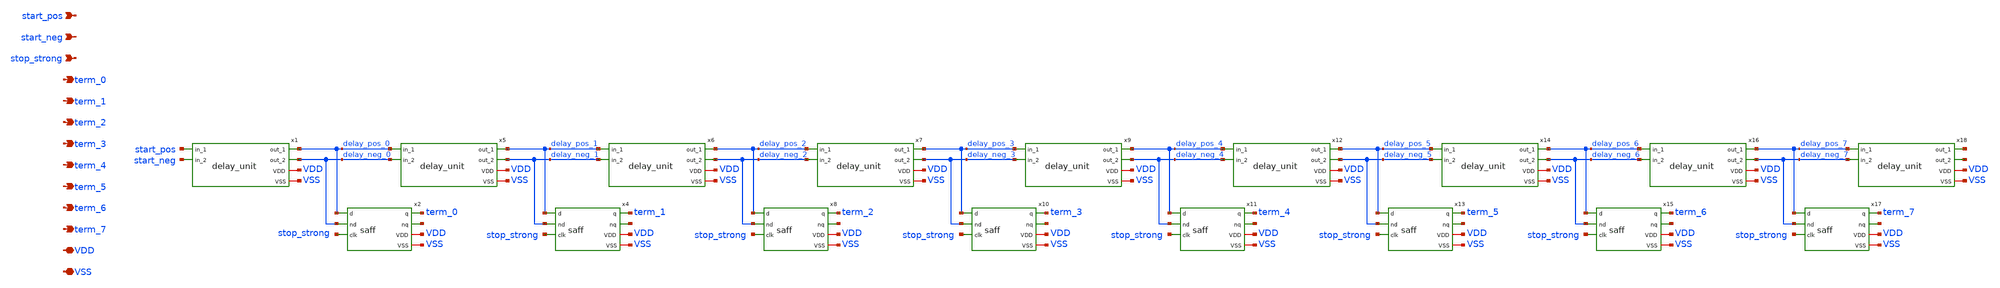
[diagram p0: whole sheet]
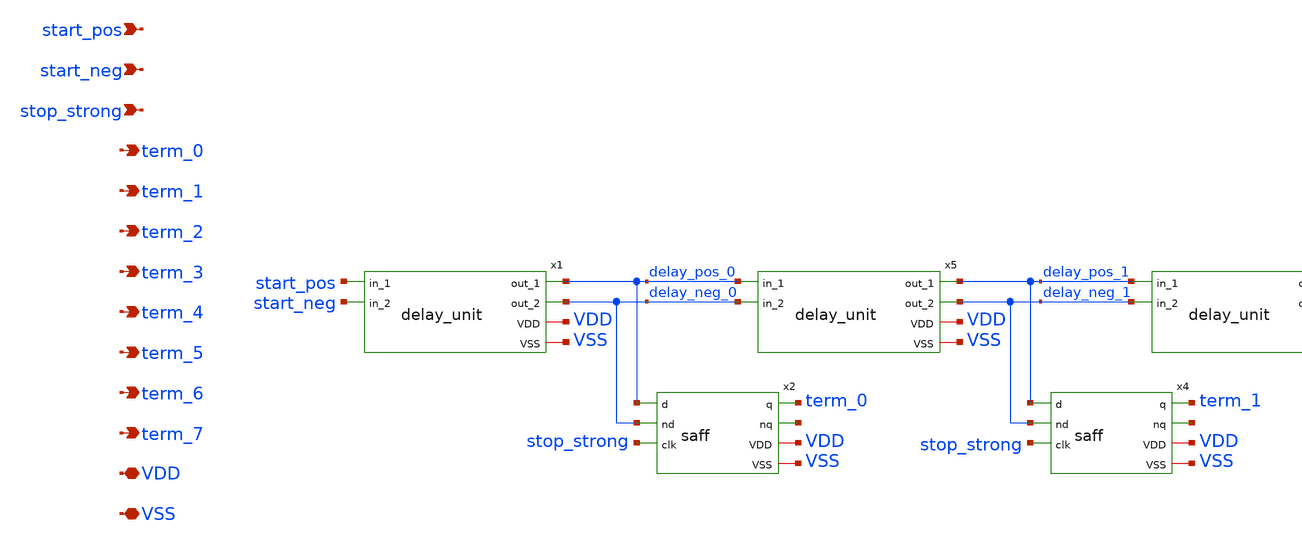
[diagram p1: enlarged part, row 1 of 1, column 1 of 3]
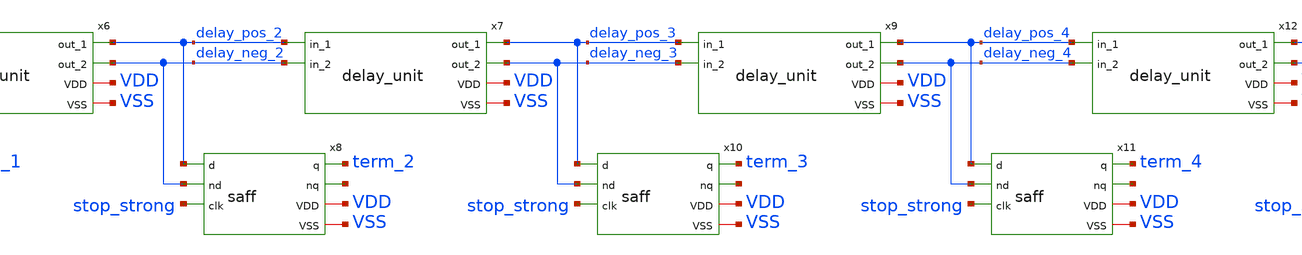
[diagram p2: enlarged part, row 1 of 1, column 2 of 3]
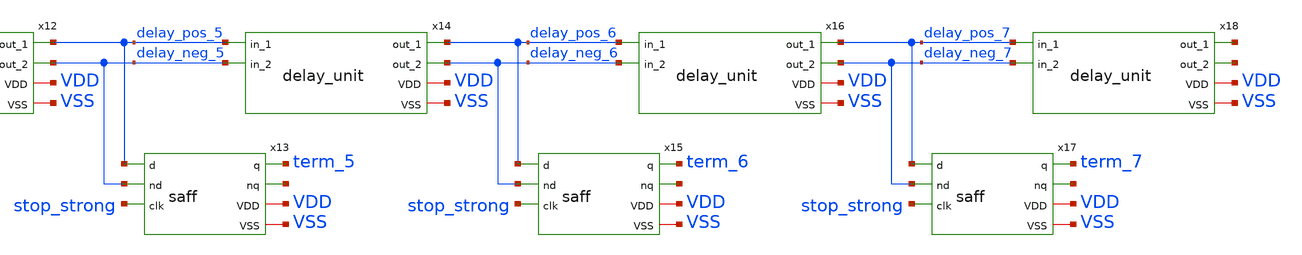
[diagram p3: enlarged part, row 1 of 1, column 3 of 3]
** sch_path: xschem/vernier_delay_line.sch
**.subckt vernier_delay_line VDD VSS start_pos stop_strong term_0 term_1 term_2 term_3 term_4 term_5
*+ term_6 term_7 start_neg
*.iopin VDD
*.iopin VSS
*.ipin start_pos
*.ipin stop_strong
*.opin term_0
*.opin term_1
*.opin term_2
*.opin term_3
*.opin term_4
*.opin term_5
*.opin term_6
*.opin term_7
*.ipin start_neg
x1 delay_pos_0 start_pos start_neg VDD delay_neg_0 VSS delay_unit
x2 delay_pos_0 delay_neg_0 stop_strong term_0 net1 VDD VSS saff
x4 delay_pos_1 delay_neg_1 stop_strong term_1 net2 VDD VSS saff
x5 delay_pos_1 delay_pos_0 delay_neg_0 VDD delay_neg_1 VSS delay_unit
x6 delay_pos_2 delay_pos_1 delay_neg_1 VDD delay_neg_2 VSS delay_unit
x7 delay_pos_3 delay_pos_2 delay_neg_2 VDD delay_neg_3 VSS delay_unit
x8 delay_pos_2 delay_neg_2 stop_strong term_2 net3 VDD VSS saff
x9 delay_pos_4 delay_pos_3 delay_neg_3 VDD delay_neg_4 VSS delay_unit
x10 delay_pos_3 delay_neg_3 stop_strong term_3 net4 VDD VSS saff
x11 delay_pos_4 delay_neg_4 stop_strong term_4 net5 VDD VSS saff
x12 delay_pos_5 delay_pos_4 delay_neg_4 VDD delay_neg_5 VSS delay_unit
x13 delay_pos_5 delay_neg_5 stop_strong term_5 net6 VDD VSS saff
x14 delay_pos_6 delay_pos_5 delay_neg_5 VDD delay_neg_6 VSS delay_unit
x15 delay_pos_6 delay_neg_6 stop_strong term_6 net7 VDD VSS saff
x16 delay_pos_7 delay_pos_6 delay_neg_6 VDD delay_neg_7 VSS delay_unit
x17 delay_pos_7 delay_neg_7 stop_strong term_7 net8 VDD VSS saff
x18 net9 delay_pos_7 delay_neg_7 VDD net10 VSS delay_unit
**.ends

* expanding   symbol:  delay_unit.sym # of pins=6
** sym_path: xschem/delay_unit.sym
** sch_path: xschem/delay_unit.sch
.subckt delay_unit out_1 in_1 in_2 VDD out_2 VSS
*.iopin VDD
*.ipin in_1
*.opin out_1
*.iopin VSS
*.ipin in_2
*.opin out_2
XM5 out_2 in_1 VDD VDD sky130_fd_pr__pfet_01v8 L=0.15 W=9 nf=1 ad='int((nf+1)/2) * W/nf * 0.29' as='int((nf+2)/2) * W/nf * 0.29'
+ pd='2*int((nf+1)/2) * (W/nf + 0.29)' ps='2*int((nf+2)/2) * (W/nf + 0.29)' nrd='0.29 / W' nrs='0.29 / W'
+ sa=0 sb=0 sd=0 mult=1 m=1
XM7 out_2 in_1 VSS VSS sky130_fd_pr__nfet_01v8 L=0.15 W=3 nf=1 ad='int((nf+1)/2) * W/nf * 0.29' as='int((nf+2)/2) * W/nf * 0.29'
+ pd='2*int((nf+1)/2) * (W/nf + 0.29)' ps='2*int((nf+2)/2) * (W/nf + 0.29)' nrd='0.29 / W' nrs='0.29 / W'
+ sa=0 sb=0 sd=0 mult=1 m=1
XM1 out_1 in_2 VDD VDD sky130_fd_pr__pfet_01v8 L=0.15 W=9 nf=1 ad='int((nf+1)/2) * W/nf * 0.29' as='int((nf+2)/2) * W/nf * 0.29'
+ pd='2*int((nf+1)/2) * (W/nf + 0.29)' ps='2*int((nf+2)/2) * (W/nf + 0.29)' nrd='0.29 / W' nrs='0.29 / W'
+ sa=0 sb=0 sd=0 mult=1 m=1
XM2 out_1 in_2 VSS VSS sky130_fd_pr__nfet_01v8 L=0.15 W=3 nf=1 ad='int((nf+1)/2) * W/nf * 0.29' as='int((nf+2)/2) * W/nf * 0.29'
+ pd='2*int((nf+1)/2) * (W/nf + 0.29)' ps='2*int((nf+2)/2) * (W/nf + 0.29)' nrd='0.29 / W' nrs='0.29 / W'
+ sa=0 sb=0 sd=0 mult=1 m=1
XM3 in_1 in_2 VDD VDD sky130_fd_pr__pfet_01v8 L=0.15 W=3 nf=1 ad='int((nf+1)/2) * W/nf * 0.29' as='int((nf+2)/2) * W/nf * 0.29'
+ pd='2*int((nf+1)/2) * (W/nf + 0.29)' ps='2*int((nf+2)/2) * (W/nf + 0.29)' nrd='0.29 / W' nrs='0.29 / W'
+ sa=0 sb=0 sd=0 mult=1 m=1
XM4 in_1 in_2 VSS VSS sky130_fd_pr__nfet_01v8 L=0.15 W=1 nf=1 ad='int((nf+1)/2) * W/nf * 0.29' as='int((nf+2)/2) * W/nf * 0.29'
+ pd='2*int((nf+1)/2) * (W/nf + 0.29)' ps='2*int((nf+2)/2) * (W/nf + 0.29)' nrd='0.29 / W' nrs='0.29 / W'
+ sa=0 sb=0 sd=0 mult=1 m=1
XM6 in_2 in_1 VDD VDD sky130_fd_pr__pfet_01v8 L=0.15 W=3 nf=1 ad='int((nf+1)/2) * W/nf * 0.29' as='int((nf+2)/2) * W/nf * 0.29'
+ pd='2*int((nf+1)/2) * (W/nf + 0.29)' ps='2*int((nf+2)/2) * (W/nf + 0.29)' nrd='0.29 / W' nrs='0.29 / W'
+ sa=0 sb=0 sd=0 mult=1 m=1
XM8 in_2 in_1 VSS VSS sky130_fd_pr__nfet_01v8 L=0.15 W=1 nf=1 ad='int((nf+1)/2) * W/nf * 0.29' as='int((nf+2)/2) * W/nf * 0.29'
+ pd='2*int((nf+1)/2) * (W/nf + 0.29)' ps='2*int((nf+2)/2) * (W/nf + 0.29)' nrd='0.29 / W' nrs='0.29 / W'
+ sa=0 sb=0 sd=0 mult=1 m=1
.ends


* expanding   symbol:  saff.sym # of pins=7
** sym_path: xschem/saff.sym
** sch_path: xschem/saff.sch
.subckt saff d nd clk q nq VDD VSS
*.iopin VDD
*.ipin d
*.opin q
*.iopin VSS
*.ipin nd
*.ipin clk
*.opin nq
XM2 net3 q VSS VSS sky130_fd_pr__nfet_01v8 L=0.15 W=1 nf=1 ad='int((nf+1)/2) * W/nf * 0.29' as='int((nf+2)/2) * W/nf * 0.29'
+ pd='2*int((nf+1)/2) * (W/nf + 0.29)' ps='2*int((nf+2)/2) * (W/nf + 0.29)' nrd='0.29 / W' nrs='0.29 / W'
+ sa=0 sb=0 sd=0 mult=1 m=1
XM3 left_latch_1 clk VDD VDD sky130_fd_pr__pfet_01v8 L=0.15 W=3 nf=1 ad='int((nf+1)/2) * W/nf * 0.29'
+ as='int((nf+2)/2) * W/nf * 0.29' pd='2*int((nf+1)/2) * (W/nf + 0.29)' ps='2*int((nf+2)/2) * (W/nf + 0.29)'
+ nrd='0.29 / W' nrs='0.29 / W' sa=0 sb=0 sd=0 mult=1 m=1
XM4 right_latch_1 clk VDD VDD sky130_fd_pr__pfet_01v8 L=0.15 W=3 nf=1 ad='int((nf+1)/2) * W/nf * 0.29'
+ as='int((nf+2)/2) * W/nf * 0.29' pd='2*int((nf+1)/2) * (W/nf + 0.29)' ps='2*int((nf+2)/2) * (W/nf + 0.29)'
+ nrd='0.29 / W' nrs='0.29 / W' sa=0 sb=0 sd=0 mult=1 m=1
XM5 right_latch_1 left_latch_1 VDD VDD sky130_fd_pr__pfet_01v8 L=0.15 W=3 nf=1 ad='int((nf+1)/2) * W/nf * 0.29'
+ as='int((nf+2)/2) * W/nf * 0.29' pd='2*int((nf+1)/2) * (W/nf + 0.29)' ps='2*int((nf+2)/2) * (W/nf + 0.29)'
+ nrd='0.29 / W' nrs='0.29 / W' sa=0 sb=0 sd=0 mult=1 m=1
XM6 left_latch_1 right_latch_1 VDD VDD sky130_fd_pr__pfet_01v8 L=0.15 W=3 nf=1 ad='int((nf+1)/2) * W/nf * 0.29'
+ as='int((nf+2)/2) * W/nf * 0.29' pd='2*int((nf+1)/2) * (W/nf + 0.29)' ps='2*int((nf+2)/2) * (W/nf + 0.29)'
+ nrd='0.29 / W' nrs='0.29 / W' sa=0 sb=0 sd=0 mult=1 m=1
XM7 right_latch_1 left_latch_1 net7 VSS sky130_fd_pr__nfet_01v8 L=0.15 W=6 nf=1 ad='int((nf+1)/2) * W/nf * 0.29'
+ as='int((nf+2)/2) * W/nf * 0.29' pd='2*int((nf+1)/2) * (W/nf + 0.29)' ps='2*int((nf+2)/2) * (W/nf + 0.29)'
+ nrd='0.29 / W' nrs='0.29 / W' sa=0 sb=0 sd=0 mult=1 m=1
XM8 left_latch_1 right_latch_1 net5 VSS sky130_fd_pr__nfet_01v8 L=0.15 W=6 nf=1 ad='int((nf+1)/2) * W/nf * 0.29'
+ as='int((nf+2)/2) * W/nf * 0.29' pd='2*int((nf+1)/2) * (W/nf + 0.29)' ps='2*int((nf+2)/2) * (W/nf + 0.29)'
+ nrd='0.29 / W' nrs='0.29 / W' sa=0 sb=0 sd=0 mult=1 m=1
XM9 net6 clk VSS VSS sky130_fd_pr__nfet_01v8 L=0.15 W=15 nf=1 ad='int((nf+1)/2) * W/nf * 0.29' as='int((nf+2)/2) * W/nf * 0.29'
+ pd='2*int((nf+1)/2) * (W/nf + 0.29)' ps='2*int((nf+2)/2) * (W/nf + 0.29)' nrd='0.29 / W' nrs='0.29 / W'
+ sa=0 sb=0 sd=0 mult=1 m=1
XM10 net7 nd net6 VSS sky130_fd_pr__nfet_01v8 L=0.15 W=12 nf=1 ad='int((nf+1)/2) * W/nf * 0.29' as='int((nf+2)/2) * W/nf * 0.29'
+ pd='2*int((nf+1)/2) * (W/nf + 0.29)' ps='2*int((nf+2)/2) * (W/nf + 0.29)' nrd='0.29 / W' nrs='0.29 / W'
+ sa=0 sb=0 sd=0 mult=1 m=1
XM11 net5 d net6 VSS sky130_fd_pr__nfet_01v8 L=0.15 W=12 nf=1 ad='int((nf+1)/2) * W/nf * 0.29' as='int((nf+2)/2) * W/nf * 0.29'
+ pd='2*int((nf+1)/2) * (W/nf + 0.29)' ps='2*int((nf+2)/2) * (W/nf + 0.29)' nrd='0.29 / W' nrs='0.29 / W'
+ sa=0 sb=0 sd=0 mult=1 m=1
XM12 right_latch_2 left_latch_1 VDD VDD sky130_fd_pr__pfet_01v8 L=0.15 W=6 nf=1 ad='int((nf+1)/2) * W/nf * 0.29'
+ as='int((nf+2)/2) * W/nf * 0.29' pd='2*int((nf+1)/2) * (W/nf + 0.29)' ps='2*int((nf+2)/2) * (W/nf + 0.29)'
+ nrd='0.29 / W' nrs='0.29 / W' sa=0 sb=0 sd=0 mult=1 m=1
XM13 right_latch_2 left_latch_1 VSS VSS sky130_fd_pr__nfet_01v8 L=0.15 W=2 nf=1 ad='int((nf+1)/2) * W/nf * 0.29'
+ as='int((nf+2)/2) * W/nf * 0.29' pd='2*int((nf+1)/2) * (W/nf + 0.29)' ps='2*int((nf+2)/2) * (W/nf + 0.29)'
+ nrd='0.29 / W' nrs='0.29 / W' sa=0 sb=0 sd=0 mult=1 m=1
XM14 left_latch_2 right_latch_1 VDD VDD sky130_fd_pr__pfet_01v8 L=0.15 W=6 nf=1 ad='int((nf+1)/2) * W/nf * 0.29'
+ as='int((nf+2)/2) * W/nf * 0.29' pd='2*int((nf+1)/2) * (W/nf + 0.29)' ps='2*int((nf+2)/2) * (W/nf + 0.29)'
+ nrd='0.29 / W' nrs='0.29 / W' sa=0 sb=0 sd=0 mult=1 m=1
XM15 left_latch_2 right_latch_1 VSS VSS sky130_fd_pr__nfet_01v8 L=0.15 W=2 nf=1 ad='int((nf+1)/2) * W/nf * 0.29'
+ as='int((nf+2)/2) * W/nf * 0.29' pd='2*int((nf+1)/2) * (W/nf + 0.29)' ps='2*int((nf+2)/2) * (W/nf + 0.29)'
+ nrd='0.29 / W' nrs='0.29 / W' sa=0 sb=0 sd=0 mult=1 m=1
XM16 q left_latch_1 VDD VDD sky130_fd_pr__pfet_01v8 L=0.15 W=3 nf=1 ad='int((nf+1)/2) * W/nf * 0.29'
+ as='int((nf+2)/2) * W/nf * 0.29' pd='2*int((nf+1)/2) * (W/nf + 0.29)' ps='2*int((nf+2)/2) * (W/nf + 0.29)'
+ nrd='0.29 / W' nrs='0.29 / W' sa=0 sb=0 sd=0 mult=1 m=1
XM17 q left_latch_2 VSS VSS sky130_fd_pr__nfet_01v8 L=0.15 W=1 nf=1 ad='int((nf+1)/2) * W/nf * 0.29'
+ as='int((nf+2)/2) * W/nf * 0.29' pd='2*int((nf+1)/2) * (W/nf + 0.29)' ps='2*int((nf+2)/2) * (W/nf + 0.29)'
+ nrd='0.29 / W' nrs='0.29 / W' sa=0 sb=0 sd=0 mult=1 m=1
XM18 nq right_latch_1 VDD VDD sky130_fd_pr__pfet_01v8 L=0.15 W=3 nf=1 ad='int((nf+1)/2) * W/nf * 0.29'
+ as='int((nf+2)/2) * W/nf * 0.29' pd='2*int((nf+1)/2) * (W/nf + 0.29)' ps='2*int((nf+2)/2) * (W/nf + 0.29)'
+ nrd='0.29 / W' nrs='0.29 / W' sa=0 sb=0 sd=0 mult=1 m=1
XM19 nq right_latch_2 VSS VSS sky130_fd_pr__nfet_01v8 L=0.15 W=1 nf=1 ad='int((nf+1)/2) * W/nf * 0.29'
+ as='int((nf+2)/2) * W/nf * 0.29' pd='2*int((nf+1)/2) * (W/nf + 0.29)' ps='2*int((nf+2)/2) * (W/nf + 0.29)'
+ nrd='0.29 / W' nrs='0.29 / W' sa=0 sb=0 sd=0 mult=1 m=1
XM20 net2 q VDD VDD sky130_fd_pr__pfet_01v8 L=0.15 W=3 nf=1 ad='int((nf+1)/2) * W/nf * 0.29' as='int((nf+2)/2) * W/nf * 0.29'
+ pd='2*int((nf+1)/2) * (W/nf + 0.29)' ps='2*int((nf+2)/2) * (W/nf + 0.29)' nrd='0.29 / W' nrs='0.29 / W'
+ sa=0 sb=0 sd=0 mult=1 m=1
XM21 nq right_latch_2 net2 VDD sky130_fd_pr__pfet_01v8 L=0.15 W=3 nf=1 ad='int((nf+1)/2) * W/nf * 0.29'
+ as='int((nf+2)/2) * W/nf * 0.29' pd='2*int((nf+1)/2) * (W/nf + 0.29)' ps='2*int((nf+2)/2) * (W/nf + 0.29)'
+ nrd='0.29 / W' nrs='0.29 / W' sa=0 sb=0 sd=0 mult=1 m=1
XM22 q left_latch_2 net1 VDD sky130_fd_pr__pfet_01v8 L=0.15 W=3 nf=1 ad='int((nf+1)/2) * W/nf * 0.29'
+ as='int((nf+2)/2) * W/nf * 0.29' pd='2*int((nf+1)/2) * (W/nf + 0.29)' ps='2*int((nf+2)/2) * (W/nf + 0.29)'
+ nrd='0.29 / W' nrs='0.29 / W' sa=0 sb=0 sd=0 mult=1 m=1
XM23 net1 nq VDD VDD sky130_fd_pr__pfet_01v8 L=0.15 W=3 nf=1 ad='int((nf+1)/2) * W/nf * 0.29' as='int((nf+2)/2) * W/nf * 0.29'
+ pd='2*int((nf+1)/2) * (W/nf + 0.29)' ps='2*int((nf+2)/2) * (W/nf + 0.29)' nrd='0.29 / W' nrs='0.29 / W'
+ sa=0 sb=0 sd=0 mult=1 m=1
XM24 q left_latch_1 net4 VSS sky130_fd_pr__nfet_01v8 L=0.15 W=1 nf=1 ad='int((nf+1)/2) * W/nf * 0.29'
+ as='int((nf+2)/2) * W/nf * 0.29' pd='2*int((nf+1)/2) * (W/nf + 0.29)' ps='2*int((nf+2)/2) * (W/nf + 0.29)'
+ nrd='0.29 / W' nrs='0.29 / W' sa=0 sb=0 sd=0 mult=1 m=1
XM25 nq right_latch_1 net3 VSS sky130_fd_pr__nfet_01v8 L=0.15 W=1 nf=1 ad='int((nf+1)/2) * W/nf * 0.29'
+ as='int((nf+2)/2) * W/nf * 0.29' pd='2*int((nf+1)/2) * (W/nf + 0.29)' ps='2*int((nf+2)/2) * (W/nf + 0.29)'
+ nrd='0.29 / W' nrs='0.29 / W' sa=0 sb=0 sd=0 mult=1 m=1
XM26 net4 nq VSS VSS sky130_fd_pr__nfet_01v8 L=0.15 W=1 nf=1 ad='int((nf+1)/2) * W/nf * 0.29' as='int((nf+2)/2) * W/nf * 0.29'
+ pd='2*int((nf+1)/2) * (W/nf + 0.29)' ps='2*int((nf+2)/2) * (W/nf + 0.29)' nrd='0.29 / W' nrs='0.29 / W'
+ sa=0 sb=0 sd=0 mult=1 m=1
.ends

.end
